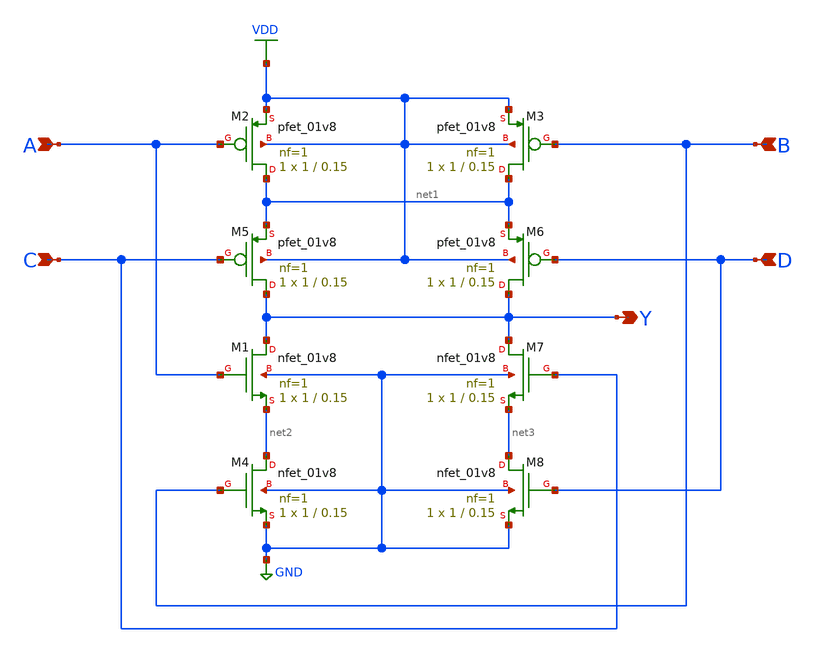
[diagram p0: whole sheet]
** sch_path: library/xschem/aoi22.sch
**.subckt aoi22 Y C D A B
*.opin Y
*.ipin C
*.ipin D
*.ipin A
*.ipin B
XM1 Y A net2 GND sky130_fd_pr__nfet_01v8 L=0.15 W=1 nf=1 ad='int((nf+1)/2) * W/nf * 0.29' as='int((nf+2)/2) * W/nf * 0.29'
+ pd='2*int((nf+1)/2) * (W/nf + 0.29)' ps='2*int((nf+2)/2) * (W/nf + 0.29)' nrd='0.29 / W' nrs='0.29 / W'
+ sa=0 sb=0 sd=0 mult=1 m=1
XM2 net1 A VDD VDD sky130_fd_pr__pfet_01v8 L=0.15 W=1 nf=1 ad='int((nf+1)/2) * W/nf * 0.29' as='int((nf+2)/2) * W/nf * 0.29'
+ pd='2*int((nf+1)/2) * (W/nf + 0.29)' ps='2*int((nf+2)/2) * (W/nf + 0.29)' nrd='0.29 / W' nrs='0.29 / W'
+ sa=0 sb=0 sd=0 mult=1 m=1
XM4 net2 B GND GND sky130_fd_pr__nfet_01v8 L=0.15 W=1 nf=1 ad='int((nf+1)/2) * W/nf * 0.29' as='int((nf+2)/2) * W/nf * 0.29'
+ pd='2*int((nf+1)/2) * (W/nf + 0.29)' ps='2*int((nf+2)/2) * (W/nf + 0.29)' nrd='0.29 / W' nrs='0.29 / W'
+ sa=0 sb=0 sd=0 mult=1 m=1
XM3 net1 B VDD VDD sky130_fd_pr__pfet_01v8 L=0.15 W=1 nf=1 ad='int((nf+1)/2) * W/nf * 0.29' as='int((nf+2)/2) * W/nf * 0.29'
+ pd='2*int((nf+1)/2) * (W/nf + 0.29)' ps='2*int((nf+2)/2) * (W/nf + 0.29)' nrd='0.29 / W' nrs='0.29 / W'
+ sa=0 sb=0 sd=0 mult=1 m=1
XM5 Y C net1 VDD sky130_fd_pr__pfet_01v8 L=0.15 W=1 nf=1 ad='int((nf+1)/2) * W/nf * 0.29' as='int((nf+2)/2) * W/nf * 0.29'
+ pd='2*int((nf+1)/2) * (W/nf + 0.29)' ps='2*int((nf+2)/2) * (W/nf + 0.29)' nrd='0.29 / W' nrs='0.29 / W'
+ sa=0 sb=0 sd=0 mult=1 m=1
XM6 Y D net1 VDD sky130_fd_pr__pfet_01v8 L=0.15 W=1 nf=1 ad='int((nf+1)/2) * W/nf * 0.29' as='int((nf+2)/2) * W/nf * 0.29'
+ pd='2*int((nf+1)/2) * (W/nf + 0.29)' ps='2*int((nf+2)/2) * (W/nf + 0.29)' nrd='0.29 / W' nrs='0.29 / W'
+ sa=0 sb=0 sd=0 mult=1 m=1
XM7 Y C net3 GND sky130_fd_pr__nfet_01v8 L=0.15 W=1 nf=1 ad='int((nf+1)/2) * W/nf * 0.29' as='int((nf+2)/2) * W/nf * 0.29'
+ pd='2*int((nf+1)/2) * (W/nf + 0.29)' ps='2*int((nf+2)/2) * (W/nf + 0.29)' nrd='0.29 / W' nrs='0.29 / W'
+ sa=0 sb=0 sd=0 mult=1 m=1
XM8 net3 D GND GND sky130_fd_pr__nfet_01v8 L=0.15 W=1 nf=1 ad='int((nf+1)/2) * W/nf * 0.29' as='int((nf+2)/2) * W/nf * 0.29'
+ pd='2*int((nf+1)/2) * (W/nf + 0.29)' ps='2*int((nf+2)/2) * (W/nf + 0.29)' nrd='0.29 / W' nrs='0.29 / W'
+ sa=0 sb=0 sd=0 mult=1 m=1
**.ends
.GLOBAL VDD
.GLOBAL GND
.end
